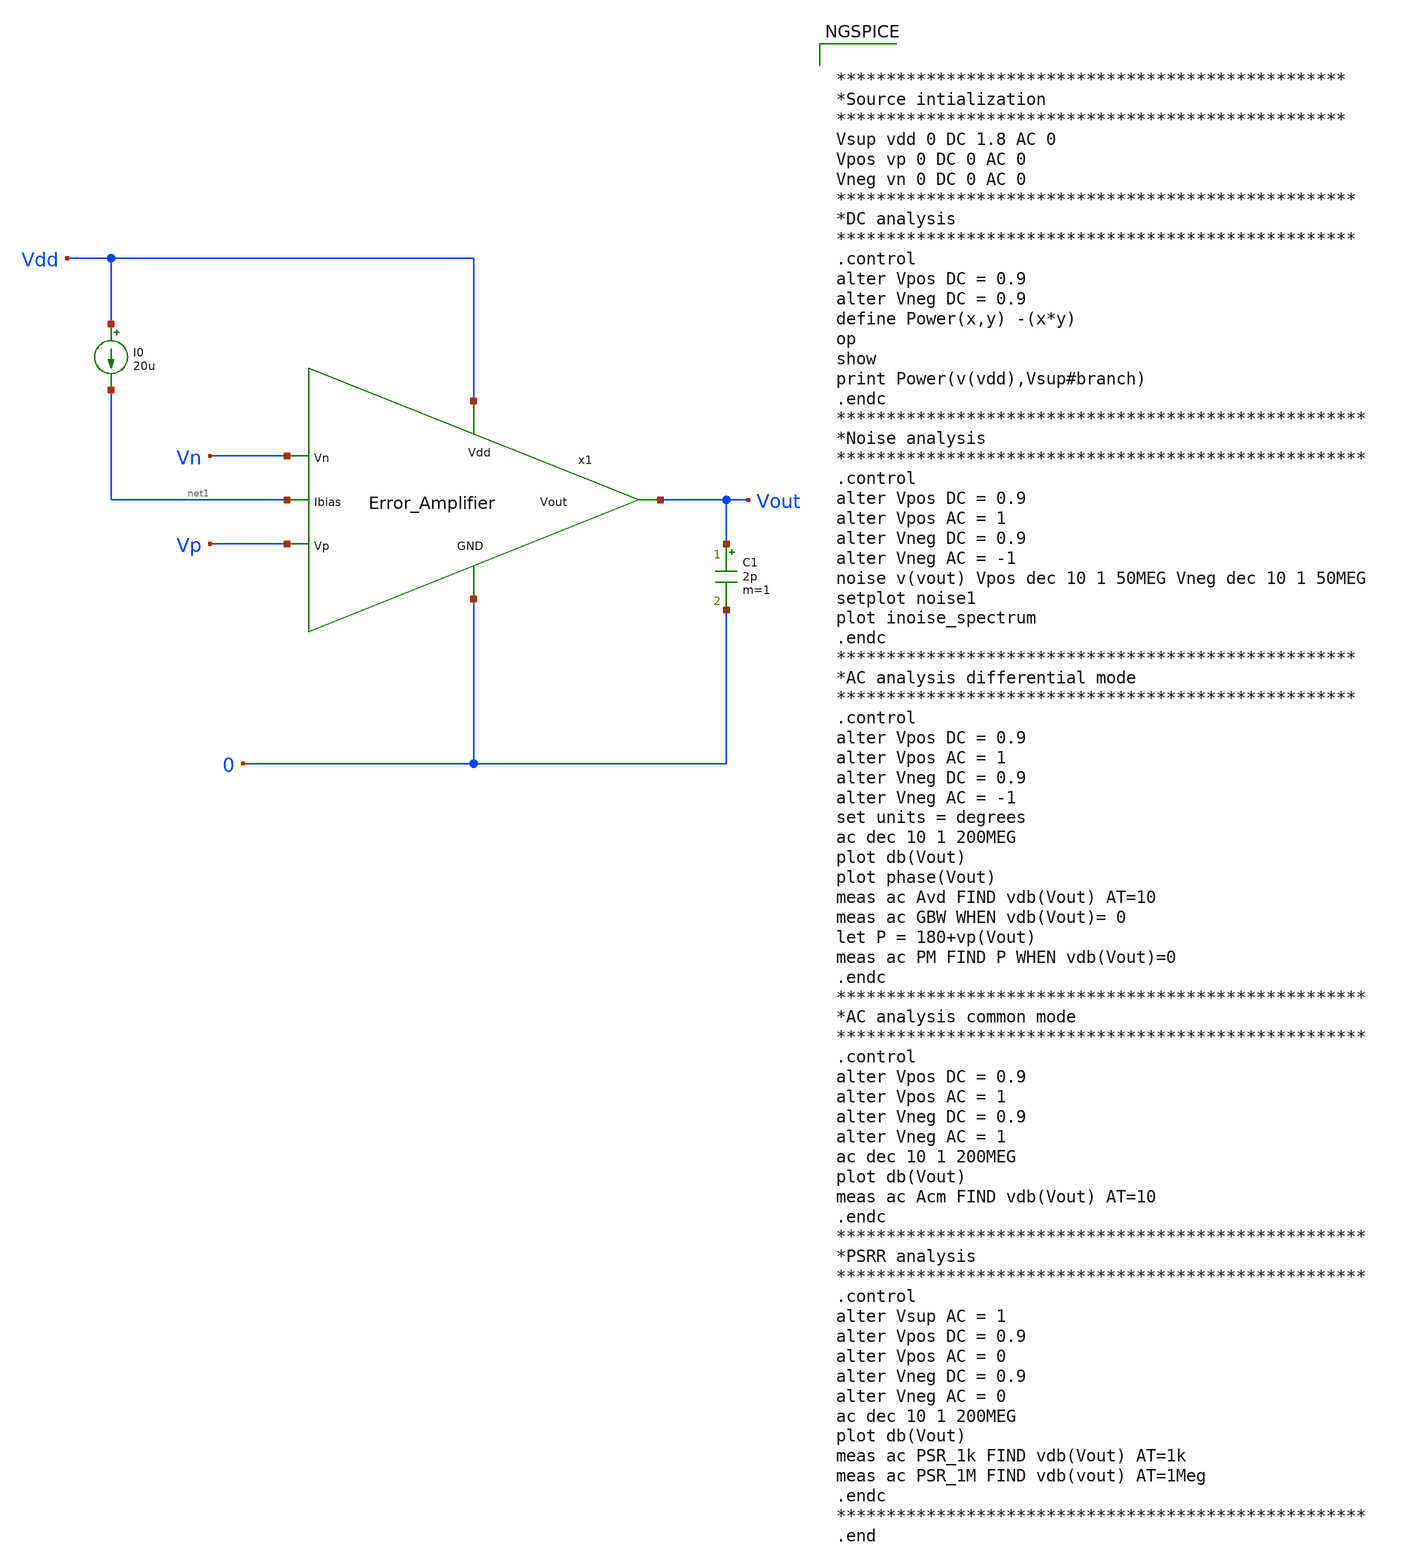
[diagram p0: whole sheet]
** sch_path: Analog_blocks/Analog_Blocks/OTA/Testbench/Miller_OTA/Transistor5v/Error_amplifier_Miller_TB.sch
**.subckt Error_amplifier_Miller_TB
I0 Vdd net1 20u
C1 Vout 0 2p m=1
x1 Vdd Vn Vp Vout net1 0 Error_Amplifier
**** begin user architecture code


***************************************************
*Source intialization
***************************************************
Vsup vdd 0 DC 1.8 AC 0
Vpos vp 0 DC 0 AC 0
Vneg vn 0 DC 0 AC 0
****************************************************
*DC analysis
****************************************************
.control
alter Vpos DC = 0.9
alter Vneg DC = 0.9
define Power(x,y) -(x*y)
op
show
print Power(v(vdd),Vsup#branch)
.endc
*****************************************************
*Noise analysis
*****************************************************
.control
alter Vpos DC = 0.9
alter Vpos AC = 1
alter Vneg DC = 0.9
alter Vneg AC = -1
noise v(vout) Vpos dec 10 1 50MEG Vneg dec 10 1 50MEG
setplot noise1
plot inoise_spectrum
.endc
****************************************************
*AC analysis differential mode
****************************************************
.control
alter Vpos DC = 0.9
alter Vpos AC = 1
alter Vneg DC = 0.9
alter Vneg AC = -1
set units = degrees
ac dec 10 1 200MEG
plot db(Vout)
plot phase(Vout)
meas ac Avd FIND vdb(Vout) AT=10
meas ac GBW WHEN vdb(Vout)= 0
let P = 180+vp(Vout)
meas ac PM FIND P WHEN vdb(Vout)=0
.endc
*****************************************************
*AC analysis common mode
*****************************************************
.control
alter Vpos DC = 0.9
alter Vpos AC = 1
alter Vneg DC = 0.9
alter Vneg AC = 1
ac dec 10 1 200MEG
plot db(Vout)
meas ac Acm FIND vdb(Vout) AT=10
.endc
*****************************************************
*PSRR analysis
*****************************************************
.control
alter Vsup AC = 1
alter Vpos DC = 0.9
alter Vpos AC = 0
alter Vneg DC = 0.9
alter Vneg AC = 0
ac dec 10 1 200MEG
plot db(Vout)
meas ac PSR_1k FIND vdb(Vout) AT=1k
meas ac PSR_1M FIND vdb(vout) AT=1Meg
.endc
*****************************************************
.end




.param mc_mm_switch=0
.param mc_pr_switch=0
.include ~/mabrains/Analog_blocks/models/sky130A/libs.ref/sky130_fd_pr/spice/sky130_fd_pr__nfet_01v8__tt.corner.spice
.include ~/mabrains/Analog_blocks/models/sky130A/libs.ref/sky130_fd_pr/spice/sky130_fd_pr__nfet_01v8_lvt__tt.corner.spice
.include ~/mabrains/Analog_blocks/models/sky130A/libs.ref/sky130_fd_pr/spice/sky130_fd_pr__pfet_01v8__tt.corner.spice
.include ~/mabrains/Analog_blocks/models/sky130A/libs.ref/sky130_fd_pr/spice/sky130_fd_pr__nfet_03v3_nvt__tt.corner.spice
.include ~/mabrains/Analog_blocks/models/sky130A/libs.ref/sky130_fd_pr/spice/sky130_fd_pr__nfet_05v0_nvt__tt.corner.spice
.include ~/mabrains/Analog_blocks/models/sky130A/libs.ref/sky130_fd_pr/spice/sky130_fd_pr__esd_nfet_01v8__tt.corner.spice
.include ~/mabrains/Analog_blocks/models/sky130A/libs.ref/sky130_fd_pr/spice/sky130_fd_pr__pfet_01v8_lvt__tt.corner.spice
.include ~/mabrains/Analog_blocks/models/sky130A/libs.ref/sky130_fd_pr/spice/sky130_fd_pr__pfet_01v8_hvt__tt.corner.spice
.include ~/mabrains/Analog_blocks/models/sky130A/libs.ref/sky130_fd_pr/spice/sky130_fd_pr__esd_pfet_g5v0d10v5__tt.corner.spice
.include ~/mabrains/Analog_blocks/models/sky130A/libs.ref/sky130_fd_pr/spice/sky130_fd_pr__pfet_g5v0d10v5__tt.corner.spice
.include ~/mabrains/Analog_blocks/models/sky130A/libs.ref/sky130_fd_pr/spice/sky130_fd_pr__pfet_g5v0d16v0__tt.corner.spice
.include ~/mabrains/Analog_blocks/models/sky130A/libs.ref/sky130_fd_pr/spice/sky130_fd_pr__nfet_g5v0d10v5__tt.corner.spice
.include ~/mabrains/Analog_blocks/models/sky130A/libs.ref/sky130_fd_pr/spice/sky130_fd_pr__nfet_g5v0d16v0__tt_discrete.corner.spice
.include ~/mabrains/Analog_blocks/models/sky130A/libs.ref/sky130_fd_pr/spice/sky130_fd_pr__esd_nfet_g5v0d10v5__tt.corner.spice
.include ~/mabrains/Analog_blocks/models/sky130A/libs.tech/ngspice/corners/tt/nonfet.spice
* Mismatch parameters
.include ~/mabrains/Analog_blocks/models/sky130A/libs.ref/sky130_fd_pr/spice/sky130_fd_pr__nfet_01v8__mismatch.corner.spice
.include ~/mabrains/Analog_blocks/models/sky130A/libs.ref/sky130_fd_pr/spice/sky130_fd_pr__pfet_01v8__mismatch.corner.spice
.include ~/mabrains/Analog_blocks/models/sky130A/libs.ref/sky130_fd_pr/spice/sky130_fd_pr__nfet_01v8_lvt__mismatch.corner.spice
.include ~/mabrains/Analog_blocks/models/sky130A/libs.ref/sky130_fd_pr/spice/sky130_fd_pr__pfet_01v8_lvt__mismatch.corner.spice
.include ~/mabrains/Analog_blocks/models/sky130A/libs.ref/sky130_fd_pr/spice/sky130_fd_pr__pfet_01v8_hvt__mismatch.corner.spice
.include ~/mabrains/Analog_blocks/models/sky130A/libs.ref/sky130_fd_pr/spice/sky130_fd_pr__nfet_g5v0d10v5__mismatch.corner.spice
.include ~/mabrains/Analog_blocks/models/sky130A/libs.ref/sky130_fd_pr/spice/sky130_fd_pr__pfet_g5v0d10v5__mismatch.corner.spice
.include ~/mabrains/Analog_blocks/models/sky130A/libs.ref/sky130_fd_pr/spice/sky130_fd_pr__nfet_05v0_nvt__mismatch.corner.spice
.include ~/mabrains/Analog_blocks/models/sky130A/libs.ref/sky130_fd_pr/spice/sky130_fd_pr__nfet_03v3_nvt__mismatch.corner.spice
* Resistor/Capacitor
.include ~/mabrains/Analog_blocks/models/sky130A/libs.tech/ngspice/r+c/res_typical__cap_typical.spice
.include ~/mabrains/Analog_blocks/models/sky130A/libs.tech/ngspice/r+c/res_typical__cap_typical__lin.spice
* Special cells
.include ~/mabrains/Analog_blocks/models/sky130A/libs.tech/ngspice/corners/tt/specialized_cells.spice
* All models
.include ~/mabrains/Analog_blocks/models/sky130A/libs.tech/ngspice/all.spice
* Corner
.include ~/mabrains/Analog_blocks/models/sky130A/libs.tech/ngspice/corners/tt/rf.spice



**** end user architecture code
**.ends
.end
